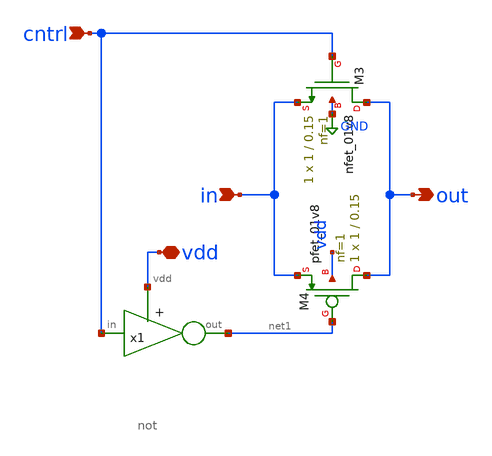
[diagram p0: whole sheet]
** sch_path: designs/subcells/core_switch/switch.sch
**.subckt switch cntrl in vdd out
*.ipin cntrl
*.ipin in
*.iopin vdd
*.opin out
XM3 out cntrl in GND sky130_fd_pr__nfet_01v8 L=0.15 W=1 nf=1 ad='int((1 + 1)/2) * 1 / 1 * 0.29' as='int((1 + 2)/2) * 1 / 1 * 0.29'
+ pd='2*int((1 + 1)/2) * (1 / 1 + 0.29)' ps='2*int((1 + 2)/2) * (1 / 1 + 0.29)' nrd='0.29 / 1 ' nrs='0.29 / 1 '
+ sa=0 sb=0 sd=0 mult=1 m=1
XM4 out net1 in vdd sky130_fd_pr__pfet_01v8 L=0.15 W=1 nf=1 ad='int((nf+1)/2) * W/nf * 0.29' as='int((nf+2)/2) * W/nf * 0.29'
+ pd='2*int((nf+1)/2) * (W/nf + 0.29)' ps='2*int((nf+2)/2) * (W/nf + 0.29)' nrd='0.29 / W' nrs='0.29 / W'
+ sa=0 sb=0 sd=0 mult=1 m=1
x1 vdd cntrl net1 not
**.ends

* expanding   symbol:  /foss/designs/spike_130/designs/subcells/core_not/not.sym # of pins=3
** sym_path: designs/subcells/core_not/not.sym
** sch_path: designs/subcells/core_not/not.sch
.subckt not vdd in out
*.ipin in
*.opin out
*.iopin vdd
XM10 out in vdd vdd sky130_fd_pr__pfet_01v8_lvt L=0.35 W=1 nf=1 ad='int((1 + 1)/2) * 1 / 1 * 0.29' as='int((1 + 2)/2) * 1 / 1 * 0.29'
+ pd='2*int((1 + 1)/2) * (1 / 1 + 0.29)' ps='2*int((1 + 2)/2) * (1 / 1 + 0.29)' nrd='0.29 / 1 ' nrs='0.29 / 1 '
+ sa=0 sb=0 sd=0 mult=1 m=1
XM1 out in GND GND sky130_fd_pr__nfet_01v8_lvt L=0.15 W=1 nf=1 ad='int((1 + 1)/2) * 1 / 1 * 0.29' as='int((1 + 2)/2) * 1 / 1 * 0.29'
+ pd='2*int((1 + 1)/2) * (1 / 1 + 0.29)' ps='2*int((1 + 2)/2) * (1 / 1 + 0.29)' nrd='0.29 / 1 ' nrs='0.29 / 1 '
+ sa=0 sb=0 sd=0 mult=1 m=1
.ends

.GLOBAL GND
.end
